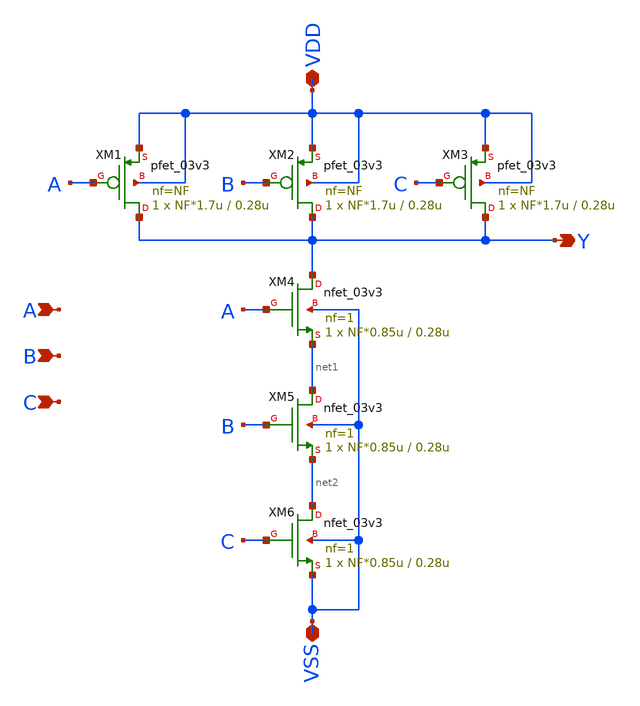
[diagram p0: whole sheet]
** sch_path: xschem_lib/DFFRAM_full_custom/nand_3in.sch
**.subckt nand_3in VDD Y VSS A B C
*.iopin VDD
*.opin Y
*.iopin VSS
*.ipin A
*.ipin B
*.ipin C
XM1 Y A VDD VDD pfet_03v3 L=0.28u W=NF*1.7u nf=NF ad='int((nf+1)/2) * W/nf * 0.18u' as='int((nf+2)/2) * W/nf * 0.18u'
+ pd='2*int((nf+1)/2) * (W/nf + 0.18u)' ps='2*int((nf+2)/2) * (W/nf + 0.18u)' nrd='0.18u / W' nrs='0.18u / W'
+ sa=0 sb=0 sd=0 m=1
XM4 Y A net1 VSS nfet_03v3 L=0.28u W=NF*0.85u nf=1 ad='int((nf+1)/2) * W/nf * 0.18u' as='int((nf+2)/2) * W/nf * 0.18u'
+ pd='2*int((nf+1)/2) * (W/nf + 0.18u)' ps='2*int((nf+2)/2) * (W/nf + 0.18u)' nrd='0.18u / W' nrs='0.18u / W'
+ sa=0 sb=0 sd=0 m=1
XM5 net1 B net2 VSS nfet_03v3 L=0.28u W=NF*0.85u nf=1 ad='int((nf+1)/2) * W/nf * 0.18u' as='int((nf+2)/2) * W/nf * 0.18u'
+ pd='2*int((nf+1)/2) * (W/nf + 0.18u)' ps='2*int((nf+2)/2) * (W/nf + 0.18u)' nrd='0.18u / W' nrs='0.18u / W'
+ sa=0 sb=0 sd=0 m=1
XM6 net2 C VSS VSS nfet_03v3 L=0.28u W=NF*0.85u nf=1 ad='int((nf+1)/2) * W/nf * 0.18u' as='int((nf+2)/2) * W/nf * 0.18u'
+ pd='2*int((nf+1)/2) * (W/nf + 0.18u)' ps='2*int((nf+2)/2) * (W/nf + 0.18u)' nrd='0.18u / W' nrs='0.18u / W'
+ sa=0 sb=0 sd=0 m=1
XM2 Y B VDD VDD pfet_03v3 L=0.28u W=NF*1.7u nf=NF ad='int((nf+1)/2) * W/nf * 0.18u' as='int((nf+2)/2) * W/nf * 0.18u'
+ pd='2*int((nf+1)/2) * (W/nf + 0.18u)' ps='2*int((nf+2)/2) * (W/nf + 0.18u)' nrd='0.18u / W' nrs='0.18u / W'
+ sa=0 sb=0 sd=0 m=1
XM3 Y C VDD VDD pfet_03v3 L=0.28u W=NF*1.7u nf=NF ad='int((nf+1)/2) * W/nf * 0.18u' as='int((nf+2)/2) * W/nf * 0.18u'
+ pd='2*int((nf+1)/2) * (W/nf + 0.18u)' ps='2*int((nf+2)/2) * (W/nf + 0.18u)' nrd='0.18u / W' nrs='0.18u / W'
+ sa=0 sb=0 sd=0 m=1
**.ends
.end
